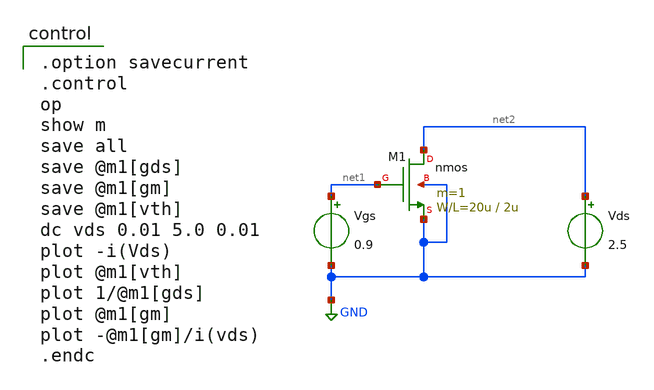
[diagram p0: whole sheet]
** sch_path: OR1/PTC06/opamp/nfet_idvds_2L.sch
**.subckt nfet_idvds_2L
Vgs net1 GND 0.9
Vds net2 GND 2.5
M1 net2 net1 GND GND nmos L=2u W=20u m=1
**** begin user architecture code
 .include $::LIB/mos.lib
.include $::LIB/passive.lib
.include $::LIB/diode.lib

.option savecurrent
.control
op
show m
save all
save @m1[gds]
save @m1[gm]
save @m1[vth]
dc vds 0.01 5.0 0.01
plot -i(Vds)
plot @m1[vth]
plot 1/@m1[gds]
plot @m1[gm]
plot -@m1[gm]/i(vds)
.endc

**** end user architecture code
**.ends
.GLOBAL GND
.end
